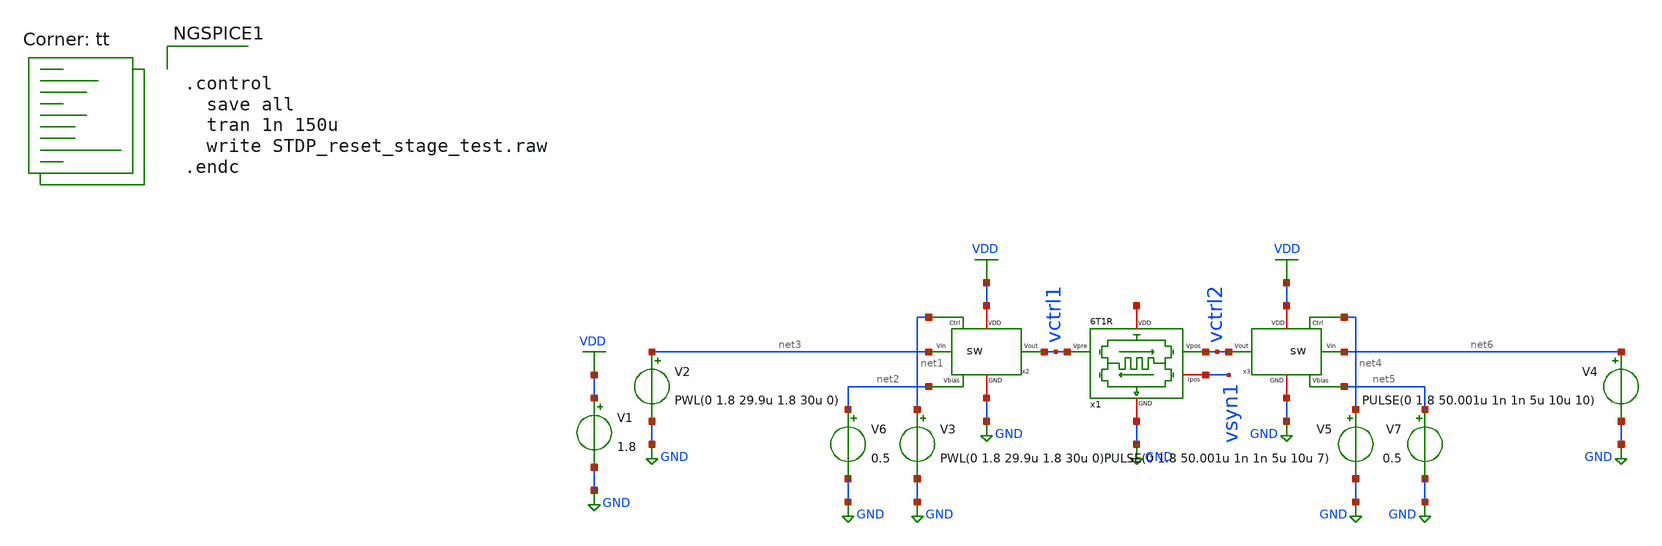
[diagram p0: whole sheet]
** sch_path: STDP/STDP_reset_stage_test.sch
**.subckt STDP_reset_stage_test
V1 VDD GND 1.8
x1 net7 vsyn1 vctrl1 vctrl2 GND 6T1R
V2 net3 GND PWL(0 1.8 29.9u 1.8 30u 0)
V3 net1 GND PWL(0 1.8 29.9u 1.8 30u 0)
x2 net2 net1 net3 GND VDD vctrl1 sw
V6 net2 GND 0.5
V4 net6 GND PULSE(0 1.8 50.001u 1n 1n 5u 10u 10)
V5 net4 GND PULSE(0 1.8 50.001u 1n 1n 5u 10u 7)
x3 net5 net4 net6 GND VDD vctrl2 sw
V7 net5 GND 0.5
**** begin user architecture code
.lib $::SKYWATER_MODELS/sky130.lib.spice tt

** opencircuitdesign pdks install
.inc $::SKYWATER_MODELS/rram_v0.spice



.control
  save all
  tran 1n 150u
  write STDP_reset_stage_test.raw
.endc


**** end user architecture code
**.ends
.GLOBAL GND
.GLOBAL VDD
.end
